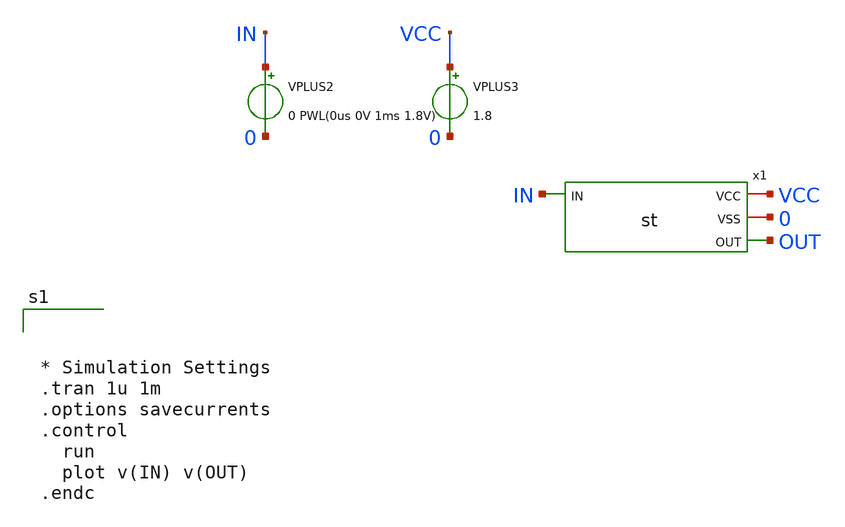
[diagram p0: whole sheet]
** sch_path: xschem/tb_st.sch
**.subckt tb_st
x1 VCC 0 IN OUT st
VPLUS3 VCC 0 1.8
VPLUS2 IN 0 0 PWL(0us 0V 1ms 1.8V)
**** begin user architecture code

** opencircuitdesign pdks install
.lib $::SKYWATER_MODELS/sky130.lib.spice tt





* Simulation Settings
.tran 1u 1m
.options savecurrents
.control
  run
  plot v(IN) v(OUT)
.endc


**** end user architecture code
**.ends

* expanding   symbol:  st.sym # of pins=4
** sym_path: xschem/st.sym
** sch_path: xschem/st.sch
.subckt st VCC VSS IN OUT
*.iopin VCC
*.iopin VSS
*.ipin IN
*.opin OUT
XM3 OUT IN VCC VCC sky130_fd_pr__pfet_01v8 L=0.15 W=1 nf=1 ad='int((nf+1)/2) * W/nf * 0.29' as='int((nf+2)/2) * W/nf * 0.29'
+ pd='2*int((nf+1)/2) * (W/nf + 0.29)' ps='2*int((nf+2)/2) * (W/nf + 0.29)' nrd='0.29 / W' nrs='0.29 / W'
+ sa=0 sb=0 sd=0 mult=1 m=1
XM5 net1 OUT VCC VCC sky130_fd_pr__pfet_01v8 L=0.15 W=1 nf=1 ad='int((nf+1)/2) * W/nf * 0.29' as='int((nf+2)/2) * W/nf * 0.29'
+ pd='2*int((nf+1)/2) * (W/nf + 0.29)' ps='2*int((nf+2)/2) * (W/nf + 0.29)' nrd='0.29 / W' nrs='0.29 / W'
+ sa=0 sb=0 sd=0 mult=1 m=1
XM6 OUT IN net2 VSS sky130_fd_pr__nfet_01v8 L=0.15 W=1 nf=1 ad='int((nf+1)/2) * W/nf * 0.29' as='int((nf+2)/2) * W/nf * 0.29'
+ pd='2*int((nf+1)/2) * (W/nf + 0.29)' ps='2*int((nf+2)/2) * (W/nf + 0.29)' nrd='0.29 / W' nrs='0.29 / W'
+ sa=0 sb=0 sd=0 mult=1 m=1
XM7 net1 OUT net2 VSS sky130_fd_pr__nfet_01v8 L=0.15 W=1 nf=1 ad='int((nf+1)/2) * W/nf * 0.29' as='int((nf+2)/2) * W/nf * 0.29'
+ pd='2*int((nf+1)/2) * (W/nf + 0.29)' ps='2*int((nf+2)/2) * (W/nf + 0.29)' nrd='0.29 / W' nrs='0.29 / W'
+ sa=0 sb=0 sd=0 mult=1 m=1
XM8 net2 net1 VSS VSS sky130_fd_pr__nfet_01v8 L=0.15 W=1 nf=1 ad='int((nf+1)/2) * W/nf * 0.29' as='int((nf+2)/2) * W/nf * 0.29'
+ pd='2*int((nf+1)/2) * (W/nf + 0.29)' ps='2*int((nf+2)/2) * (W/nf + 0.29)' nrd='0.29 / W' nrs='0.29 / W'
+ sa=0 sb=0 sd=0 mult=1 m=1
.ends

.end
